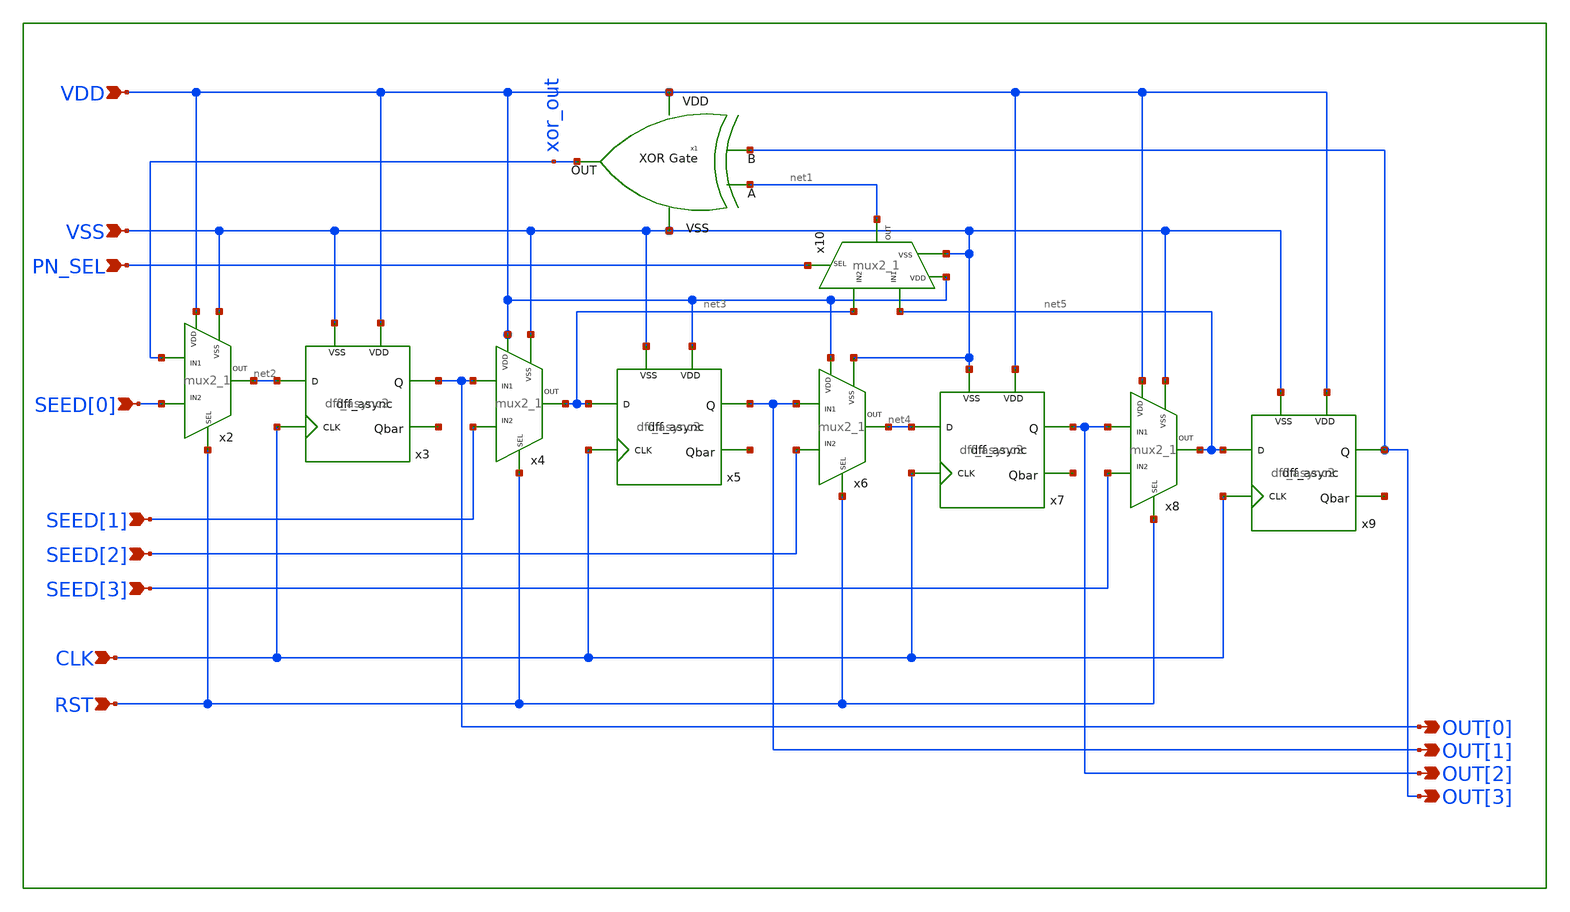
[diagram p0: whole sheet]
** sch_path: Project/1-on-chip/schematic/PNgen/pn_seqgen.sch
**.subckt pn_seqgen VDD OUT[3] VSS PN_SEL SEED[0] SEED[1] SEED[2] SEED[3] CLK RST OUT[0] OUT[1]
*+ OUT[2]
*.ipin VDD
*.opin OUT[3]
*.ipin VSS
*.ipin PN_SEL
*.ipin SEED[0]
*.ipin SEED[1]
*.ipin SEED[2]
*.ipin SEED[3]
*.ipin CLK
*.ipin RST
*.opin OUT[0]
*.opin OUT[1]
*.opin OUT[2]
x1 net1 OUT[3] VDD VSS xor_out xor
x3 net2 CLK VDD VSS OUT[0] net6 dff_async2
x5 net3 CLK VDD VSS OUT[1] net7 dff_async2
x7 net4 CLK VDD VSS OUT[2] net8 dff_async2
x9 net5 CLK VDD VSS OUT[3] net9 dff_async2
x2 VDD VSS xor_out net2 RST SEED[0] mux2_1
x4 VDD VSS OUT[0] net3 RST SEED[1] mux2_1
x6 VDD VSS OUT[1] net4 RST SEED[2] mux2_1
x8 VDD VSS OUT[2] net5 RST SEED[3] mux2_1
x10 VDD VSS net5 net1 PN_SEL net3 mux2_1
**.ends
.end
